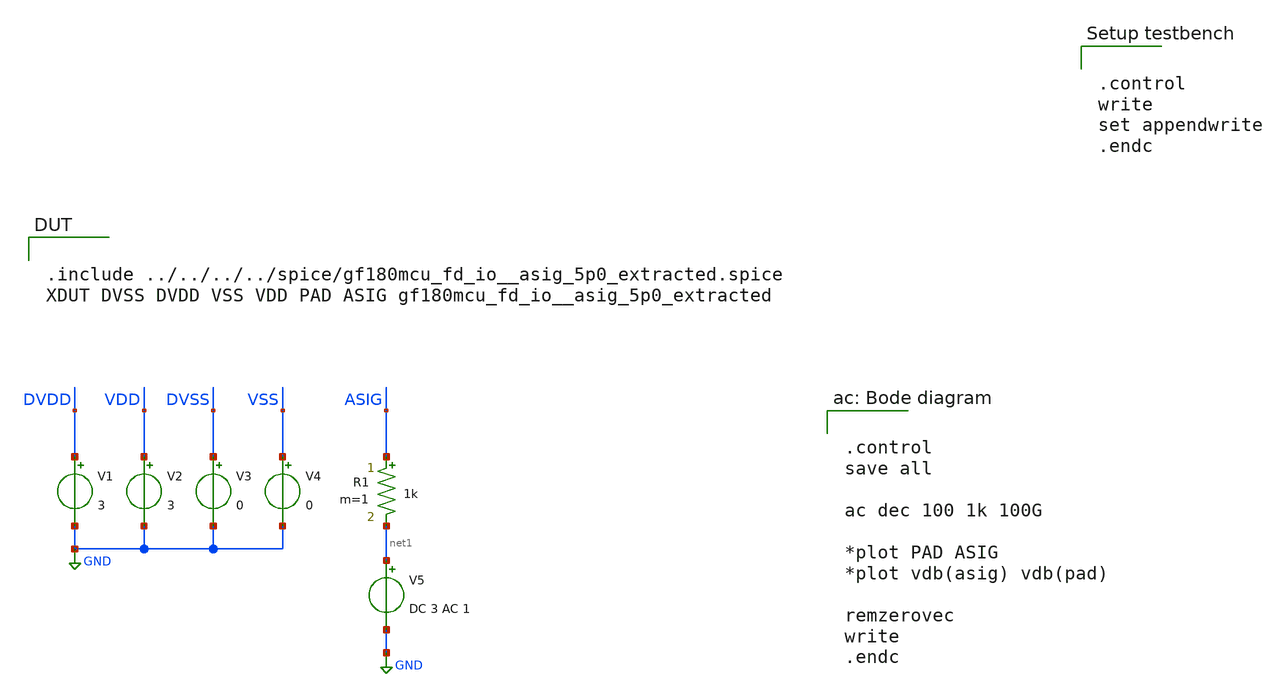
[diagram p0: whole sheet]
** sch_path: padframe/bode_asig_5p0/test/bode_asig_5p0.sch

.control
write
set appendwrite
.endc

.include $env(PDK_ROOT)/$env(PDK)/libs.tech/ngspice/design.ngspice
.lib $env(PDK_ROOT)/$env(PDK)/libs.tech/ngspice/sm141064.ngspice typical
.lib $env(PDK_ROOT)/$env(PDK)/libs.tech/ngspice/sm141064.ngspice diode_typical
.lib $env(PDK_ROOT)/$env(PDK)/libs.tech/ngspice/sm141064.ngspice res_typical
*.lib $env(PDK_ROOT)/$env(PDK)/libs.tech/ngspice/sm141064.ngspice mimcap_typical
.lib $env(PDK_ROOT)/$env(PDK)/libs.tech/ngspice/sm141064.ngspice moscap_typical
.lib $env(PDK_ROOT)/$env(PDK)/libs.tech/ngspice/sm141064.ngspice bjt_typical
*.lib $env(PDK_ROOT)/$env(PDK)/libs.tech/ngspice/sm141064.ngspice cap_mim

**.subckt bode_asig_5p0
V1 DVDD GND 3
V2 VDD GND 3
V3 DVSS GND 0
V4 VSS GND 0
V5 net1 GND DC 3 AC 1
R1 ASIG net1 1k m=1
**** begin user architecture code

.include ../../../../spice/gf180mcu_fd_io__asig_5p0_extracted.spice
XDUT DVSS DVDD VSS VDD PAD ASIG gf180mcu_fd_io__asig_5p0_extracted



.control
save all

ac dec 100 1k 100G

*plot PAD ASIG
*plot vdb(asig) vdb(pad)

remzerovec
write
.endc


**** end user architecture code
**.ends
.GLOBAL GND
.end
